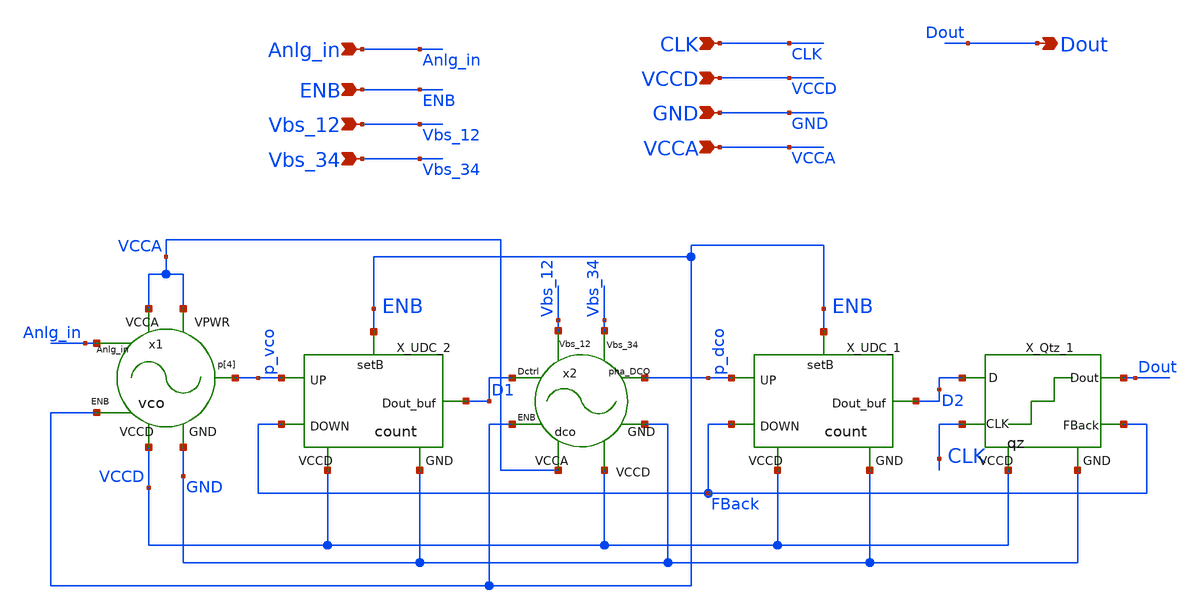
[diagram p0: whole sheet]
** sch_path: xschem/system/system.sch
**.subckt system Anlg_in ENB Vbs_12 Vbs_34 CLK VCCD GND VCCA Dout
*.ipin Anlg_in
*.ipin ENB
*.ipin Vbs_12
*.ipin Vbs_34
*.ipin CLK
*.ipin VCCD
*.ipin GND
*.ipin VCCA
*.opin Dout
x1 GND p_vco Anlg_in ENB VCCA VCCD VCCA vco
X_UDC_2 VCCD GND p_vco ENB FBack D1 count
x2 GND VCCD VCCA D1 ENB Vbs_12 Vbs_34 p_dco dco
X_UDC_1 VCCD GND p_dco ENB FBack D2 count
X_Qtz_1 VCCD GND CLK Dout FBack D2 qz
**.ends
.end
